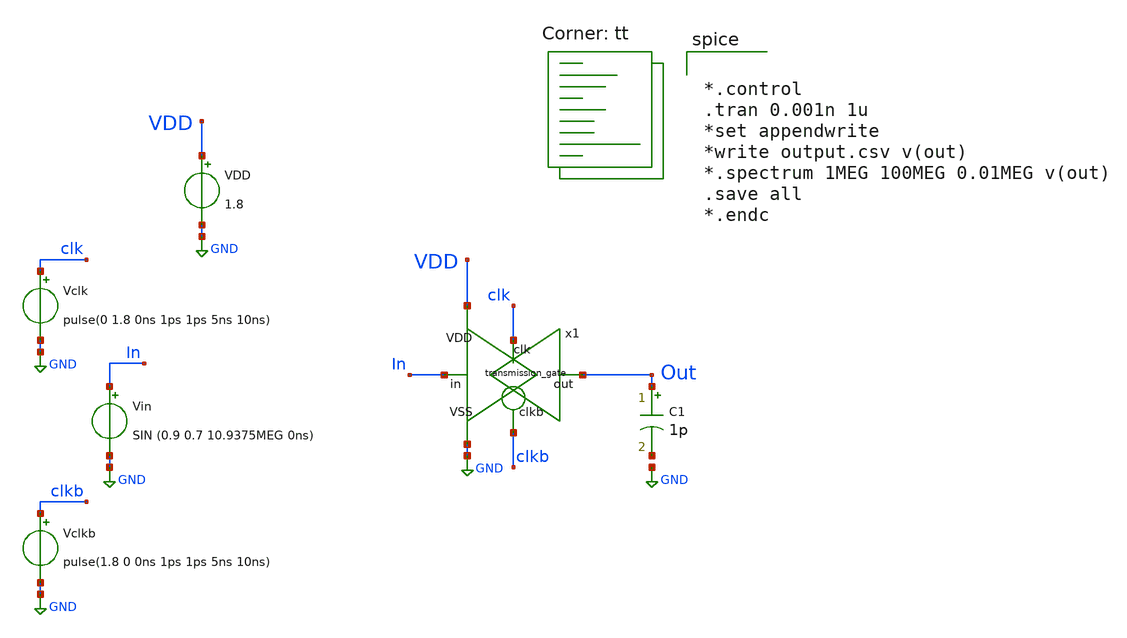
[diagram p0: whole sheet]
** sch_path: SampleHold/TG_switch.sch
**.subckt TG_switch
x1 In clkb clk VDD GND Out transmission_gate
Vclk clk GND pulse(0 1.8 0ns 1ps 1ps 5ns 10ns)
Vin In GND SIN (0.9 0.7 10.9375MEG 0ns)
C1 Out net1 1p m=1
VDD VDD GND 1.8
Vclkb clkb GND pulse(1.8 0 0ns 1ps 1ps 5ns 10ns)
**** begin user architecture code
.lib $::SKYWATER_MODELS/sky130.lib.spice tt


*.control
.tran 0.001n 1u
*set appendwrite
*write output.csv v(out)
*.spectrum 1MEG 100MEG 0.01MEG v(out)
.save all
*.endc


**** end user architecture code
**.ends

* expanding   symbol:  project/transmission_gate.sym # of pins=6
** sym_path: SampleHold/transmission_gate.sym
** sch_path: SampleHold/transmission_gate.sch
.subckt transmission_gate in clkb clk VDD VSS out
*.ipin in
*.ipin clk
*.ipin clkb
*.opin out
*.ipin VDD
*.ipin VSS
XM1 out clk in VSS sky130_fd_pr__nfet_01v8 L=0.15 W=0.5 nf=1 ad='int((nf+1)/2) * W/nf * 0.29' as='int((nf+2)/2) * W/nf * 0.29'
+ pd='2*int((nf+1)/2) * (W/nf + 0.29)' ps='2*int((nf+2)/2) * (W/nf + 0.29)' nrd='0.29 / W' nrs='0.29 / W'
+ sa=0 sb=0 sd=0 mult=1 m=1
XM2 out clkb in VDD sky130_fd_pr__pfet_01v8 L=0.15 W=0.5 nf=1 ad='int((nf+1)/2) * W/nf * 0.29' as='int((nf+2)/2) * W/nf * 0.29'
+ pd='2*int((nf+1)/2) * (W/nf + 0.29)' ps='2*int((nf+2)/2) * (W/nf + 0.29)' nrd='0.29 / W' nrs='0.29 / W'
+ sa=0 sb=0 sd=0 mult=1 m=1
.ends

.GLOBAL GND
.end
